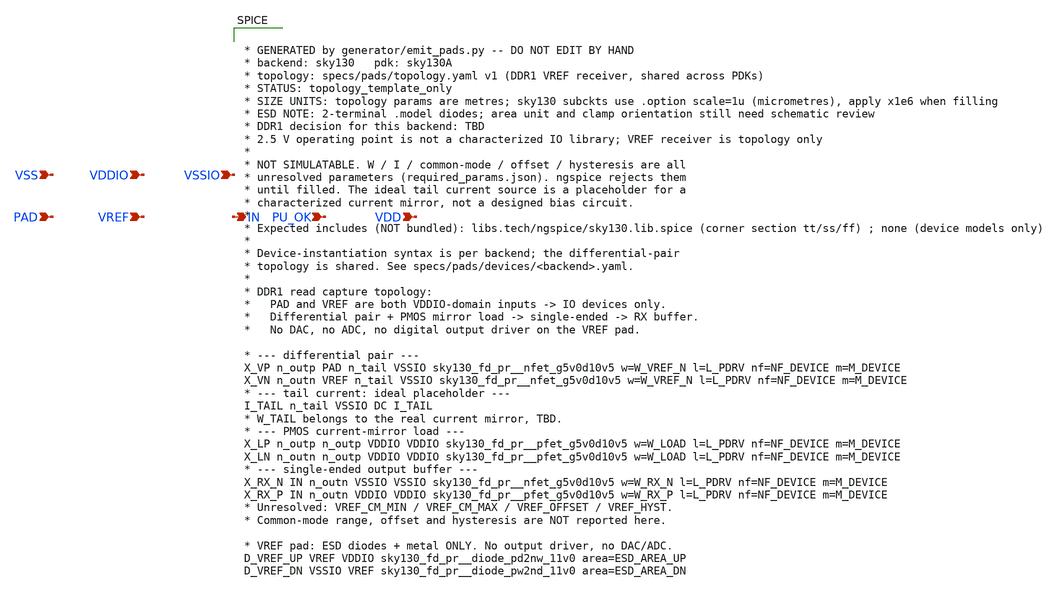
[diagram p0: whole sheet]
** sch_path: sch/pads/sky130/vref_receiver.sch
**.subckt vref_receiver PAD VREF IN PU_OK VDD VSS VDDIO VSSIO
*.ipin PAD
*.ipin VREF
*.opin IN
*.ipin PU_OK
*.ipin VDD
*.ipin VSS
*.ipin VDDIO
*.ipin VSSIO
**** begin user architecture code


* GENERATED by generator/emit_pads.py -- DO NOT EDIT BY HAND
* backend: sky130   pdk: sky130A
* topology: specs/pads/topology.yaml v1 (DDR1 VREF receiver, shared across PDKs)
* STATUS: topology_template_only
* SIZE UNITS: topology params are metres; sky130 subckts use .option scale=1u (micrometres), apply
*+ x1e6 when filling
* ESD NOTE: 2-terminal .model diodes; area unit and clamp orientation still need schematic review
* DDR1 decision for this backend: TBD
* 2.5 V operating point is not a characterized IO library; VREF receiver is topology only
*
* NOT SIMULATABLE. W / I / common-mode / offset / hysteresis are all
* unresolved parameters (required_params.json). ngspice rejects them
* until filled. The ideal tail current source is a placeholder for a
* characterized current mirror, not a designed bias circuit.
*
* Expected includes (NOT bundled): libs.tech/ngspice/sky130.lib.spice (corner section tt/ss/ff) ;
*+ none (device models only)
*
* Device-instantiation syntax is per backend; the differential-pair
* topology is shared. See specs/pads/devices/<backend>.yaml.
*
* DDR1 read capture topology:
*   PAD and VREF are both VDDIO-domain inputs -> IO devices only.
*   Differential pair + PMOS mirror load -> single-ended -> RX buffer.
*   No DAC, no ADC, no digital output driver on the VREF pad.

* --- differential pair ---
X_VP n_outp PAD n_tail VSSIO sky130_fd_pr__nfet_g5v0d10v5 w=W_VREF_N l=L_PDRV nf=NF_DEVICE
+ m=M_DEVICE
X_VN n_outn VREF n_tail VSSIO sky130_fd_pr__nfet_g5v0d10v5 w=W_VREF_N l=L_PDRV nf=NF_DEVICE
+ m=M_DEVICE
* --- tail current: ideal placeholder ---
I_TAIL n_tail VSSIO DC I_TAIL
* W_TAIL belongs to the real current mirror, TBD.
* --- PMOS current-mirror load ---
X_LP n_outp n_outp VDDIO VDDIO sky130_fd_pr__pfet_g5v0d10v5 w=W_LOAD l=L_PDRV nf=NF_DEVICE
+ m=M_DEVICE
X_LN n_outn n_outp VDDIO VDDIO sky130_fd_pr__pfet_g5v0d10v5 w=W_LOAD l=L_PDRV nf=NF_DEVICE
+ m=M_DEVICE
* --- single-ended output buffer ---
X_RX_N IN n_outn VSSIO VSSIO sky130_fd_pr__nfet_g5v0d10v5 w=W_RX_N l=L_PDRV nf=NF_DEVICE m=M_DEVICE
X_RX_P IN n_outn VDDIO VDDIO sky130_fd_pr__pfet_g5v0d10v5 w=W_RX_P l=L_PDRV nf=NF_DEVICE m=M_DEVICE
* Unresolved: VREF_CM_MIN / VREF_CM_MAX / VREF_OFFSET / VREF_HYST.
* Common-mode range, offset and hysteresis are NOT reported here.

* VREF pad: ESD diodes + metal ONLY. No output driver, no DAC/ADC.
D_VREF_UP VREF VDDIO sky130_fd_pr__diode_pd2nw_11v0 area=ESD_AREA_UP
D_VREF_DN VSSIO VREF sky130_fd_pr__diode_pw2nd_11v0 area=ESD_AREA_DN


**** end user architecture code
**.ends
.end
